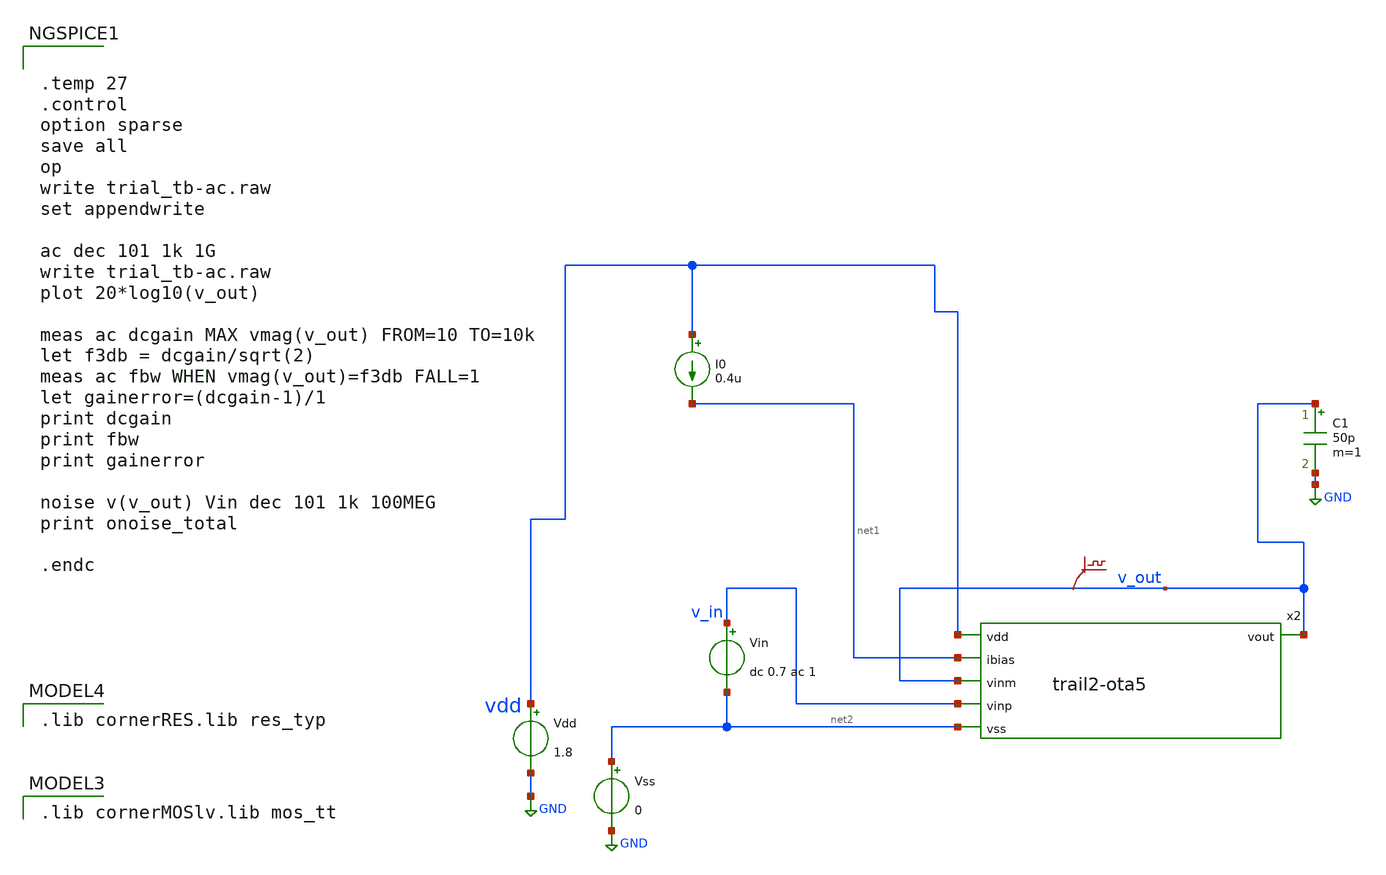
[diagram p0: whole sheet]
** sch_path: design/ota_design/trail2_ota5_tb_ac.sch
**.subckt trail2_ota5_tb_ac
Vss net2 GND 0
Vin v_in net2 dc 0.7 ac 1
C1 v_out GND 50p m=1
I0 vdd net1 0.4u
.save v(v_out)
Vdd vdd GND 1.8
x2 vdd v_out net1 v_out v_in net2 trail2-ota5
**** begin user architecture code
 .lib cornerMOSlv.lib mos_tt



.temp 27
.control
option sparse
save all
op
write trial_tb-ac.raw
set appendwrite

ac dec 101 1k 1G
write trial_tb-ac.raw
plot 20*log10(v_out)

meas ac dcgain MAX vmag(v_out) FROM=10 TO=10k
let f3db = dcgain/sqrt(2)
meas ac fbw WHEN vmag(v_out)=f3db FALL=1
let gainerror=(dcgain-1)/1
print dcgain
print fbw
print gainerror

noise v(v_out) Vin dec 101 1k 100MEG
print onoise_total

.endc


 .lib cornerRES.lib res_typ

**** end user architecture code
**.ends

* expanding   symbol:  trail2-ota5.sym # of pins=6
** sym_path: design/ota_design/trail2-ota5.sym
** sch_path: design/ota_design/trail2-ota5.sch
.subckt trail2-ota5 vdd vout ibias vinm vinp vss
*.ipin vss
*.ipin vdd
*.ipin ibias
*.ipin vinm
*.ipin vinp
*.opin vout
XM1 vout net1 vdd vdd sg13_lv_pmos w=0.22u l=0.3u ng=1 m=1 mm_ok=1
XM2 vout vinm net2 vss sg13_lv_nmos w=0.45u l=0.3u ng=1 m=1 mm_ok=1
XM3 net1 net1 vdd vdd sg13_lv_pmos w=0.22u l=0.3u ng=1 m=1 mm_ok=1
XM4 net1 vinp net2 vss sg13_lv_nmos w=0.45u l=0.3u ng=1 m=1 mm_ok=1
XM5 net2 net3 vss vss sg13_lv_nmos w=0.9u l=0.3u ng=1 m=1 mm_ok=1
XM6 net4 net3 vss vss sg13_lv_nmos w=0.9u l=0.3u ng=1 m=1 mm_ok=1
XM7 net3 net3 vss vss sg13_lv_nmos w=0.9u l=0.3u ng=1 m=1 mm_ok=1
XM8 net3 ibias ibias vdd sg13_lv_pmos w=0.44u l=0.3u ng=1 m=1 mm_ok=1
XM9 net4 ibias vdd vdd sg13_lv_pmos w=0.44u l=0.3u ng=1 m=1 mm_ok=1
.ends

.GLOBAL GND
.end
